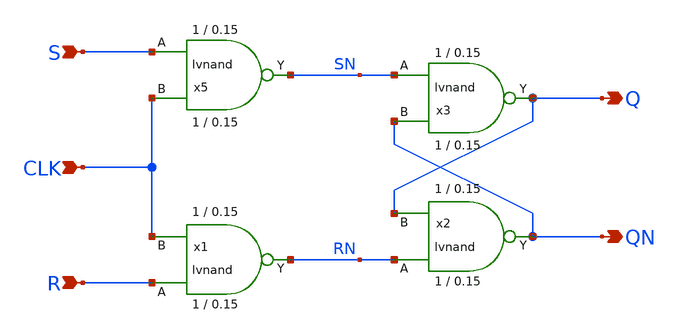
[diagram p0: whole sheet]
** sch_path: sky130A/libs.tech/xschem/sky130_tests/srlatch.sch
* Copyright 2020 Stefan Frederik Schippers
* Licensed under the Apache License, Version 2.0 (the "License");
* you may not use this file except in compliance with the License.
* You may obtain a copy of the License at
* https://www.apache.org/licenses/LICENSE-2.0
* Unless required by applicable law or agreed to in writing, software
* distributed under the License is distributed on an "AS IS" BASIS,
* WITHOUT WARRANTIES OR CONDITIONS OF ANY KIND, either express or implied.
* See the License for the specific language governing permissions and
* limitations under the License.
**.subckt srlatch S R Q QN CLK
*.ipin S
*.ipin R
*.opin Q
*.opin QN
*.ipin CLK
x5 S CLK SN VCC VSS lvnand WidthN=1 LenN=0.15 WidthP=1 LenP=0.15 m=1
x1 R CLK RN VCC VSS lvnand WidthN=1 LenN=0.15 WidthP=1 LenP=0.15 m=1
x2 RN Q QN VCC VSS lvnand WidthN=1 LenN=0.15 WidthP=1 LenP=0.15 m=1
x3 SN QN Q VCC VSS lvnand WidthN=1 LenN=0.15 WidthP=1 LenP=0.15 m=1
**** begin user architecture code

.lib $::SKYWATER_MODELS/sky130.lib.spice tt
* Mismatch parameters
* Resistor$::SKYWATER_MODELS/Capacitor
* Special cells
* All models
* Corner

**** end user architecture code
**.ends

* expanding   symbol:  sky130_tests/lvnand.sym # of pins=3
** sym_path: sky130A/libs.tech/xschem/sky130_tests/lvnand.sym
** sch_path: sky130A/libs.tech/xschem/sky130_tests/lvnand.sch
.subckt lvnand A B Y VCCPIN VSSPIN  WidthN=1 LenN=0.15 WidthP=1 LenP=0.15
*.ipin A
*.ipin B
*.opin Y
XM1 Y B S VSSPIN sky130_fd_pr__nfet_01v8 L=LenN W=WidthN nf=1 ad='int((nf+1)/2) * W/nf * 0.29' as='int((nf+2)/2) * W/nf * 0.29'
+ pd='2*int((nf+1)/2) * (W/nf + 0.29)' ps='2*int((nf+2)/2) * (W/nf + 0.29)' nrd='0.29 / W' nrs='0.29 / W'
+ sa=0 sb=0 sd=0 mult=1 m=1
XM2 Y A VCCPIN VCCPIN sky130_fd_pr__pfet_01v8 L=LenP W=WidthP nf=1 ad='int((nf+1)/2) * W/nf * 0.29' as='int((nf+2)/2) * W/nf * 0.29'
+ pd='2*int((nf+1)/2) * (W/nf + 0.29)' ps='2*int((nf+2)/2) * (W/nf + 0.29)' nrd='0.29 / W' nrs='0.29 / W'
+ sa=0 sb=0 sd=0 mult=1 m=1
XM3 Y B VCCPIN VCCPIN sky130_fd_pr__pfet_01v8 L=LenP W=WidthP nf=1 ad='int((nf+1)/2) * W/nf * 0.29' as='int((nf+2)/2) * W/nf * 0.29'
+ pd='2*int((nf+1)/2) * (W/nf + 0.29)' ps='2*int((nf+2)/2) * (W/nf + 0.29)' nrd='0.29 / W' nrs='0.29 / W'
+ sa=0 sb=0 sd=0 mult=1 m=1
XM4 S A VSSPIN VSSPIN sky130_fd_pr__nfet_01v8 L=LenN W=WidthN nf=1 ad='int((nf+1)/2) * W/nf * 0.29' as='int((nf+2)/2) * W/nf * 0.29'
+ pd='2*int((nf+1)/2) * (W/nf + 0.29)' ps='2*int((nf+2)/2) * (W/nf + 0.29)' nrd='0.29 / W' nrs='0.29 / W'
+ sa=0 sb=0 sd=0 mult=1 m=1
.ends

**** begin user architecture code

* .option SCALE=1e-6
.option method=gear seed=12
.param L=0.15
.param W=0.5

vd d 0 0
vg g 0 0
.control
dc vd 0 2 0.01 vg 0 2 0.2
alterparam L=0.18
alterparam W=1
reset
dc vd 0 2 0.01 vg 0 2 0.2
alterparam L=0.3
alterparam W=2
reset
dc vd 0 2 0.01 vg 0 2 0.2
alterparam L=0.5
alterparam W=3
reset
dc vd 0 2 0.01 vg 0 2 0.2

.endc





**** end user architecture code
.end
